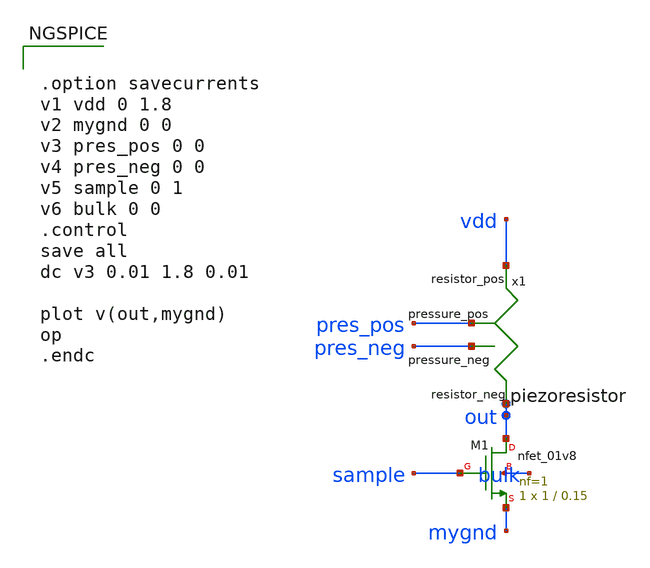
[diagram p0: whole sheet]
** sch_path: circuits/1t1r_nmos.sch
* Copyright 2020 Stefan Frederik Schippers
* Licensed under the Apache License, Version 2.0 (the "License");
* you may not use this file except in compliance with the License.
* You may obtain a copy of the License at
* https://www.apache.org/licenses/LICENSE-2.0
* Unless required by applicable law or agreed to in writing, software
* distributed under the License is distributed on an "AS IS" BASIS,
* WITHOUT WARRANTIES OR CONDITIONS OF ANY KIND, either express or implied.
* See the License for the specific language governing permissions and
* limitations under the License.
**.subckt 1t1r_nmos
x1 pres_pos pres_neg vdd out piezoresistor
XM1 out sample mygnd bulk sky130_fd_pr__nfet_01v8 L=0.15 W=1 nf=1 ad='int((nf+1)/2) * W/nf * 0.29' as='int((nf+2)/2) * W/nf * 0.29'
+ pd='2*int((nf+1)/2) * (W/nf + 0.29)' ps='2*int((nf+2)/2) * (W/nf + 0.29)' nrd='0.29 / W' nrs='0.29 / W'
+ sa=0 sb=0 sd=0 mult=1 m=1
**** begin user architecture code
 .lib $::SKYWATER_MODELS/models/sky130.lib.spice tt

.param mc_mm_switch=0
.param mc_pr_switch=1




.option savecurrents
v1 vdd 0 1.8
v2 mygnd 0 0
v3 pres_pos 0 0
v4 pres_neg 0 0
v5 sample 0 1
v6 bulk 0 0
.control
save all
dc v3 0.01 1.8 0.01

plot v(out,mygnd)
op
.endc


**** end user architecture code
**.ends

* expanding   symbol:  /home/mast/Progetti/Telluride2021/sky130_TAC3/piezoresistor.sym # of pins=4
** sym_path: circuits/piezoresistor.sym
** sch_path: circuits/piezoresistor.sch
.subckt piezoresistor pressure_pos pressure_neg resistor_pos resistor_neg
*.ipin pressure_pos
*.ipin pressure_neg
*.iopin resistor_pos
*.iopin resistor_neg
Broot sqrtp 0 V = sqrt(v(pressure_pos,pressure_neg))
Bres res 0 V = 106*(50/v(sqrtp)-1)*exp(-0.328*v(sqrtp))+15
Brvar resistor_pos resistor_neg I = V(resistor_pos,resistor_neg)/V(res)
.ends

.end
